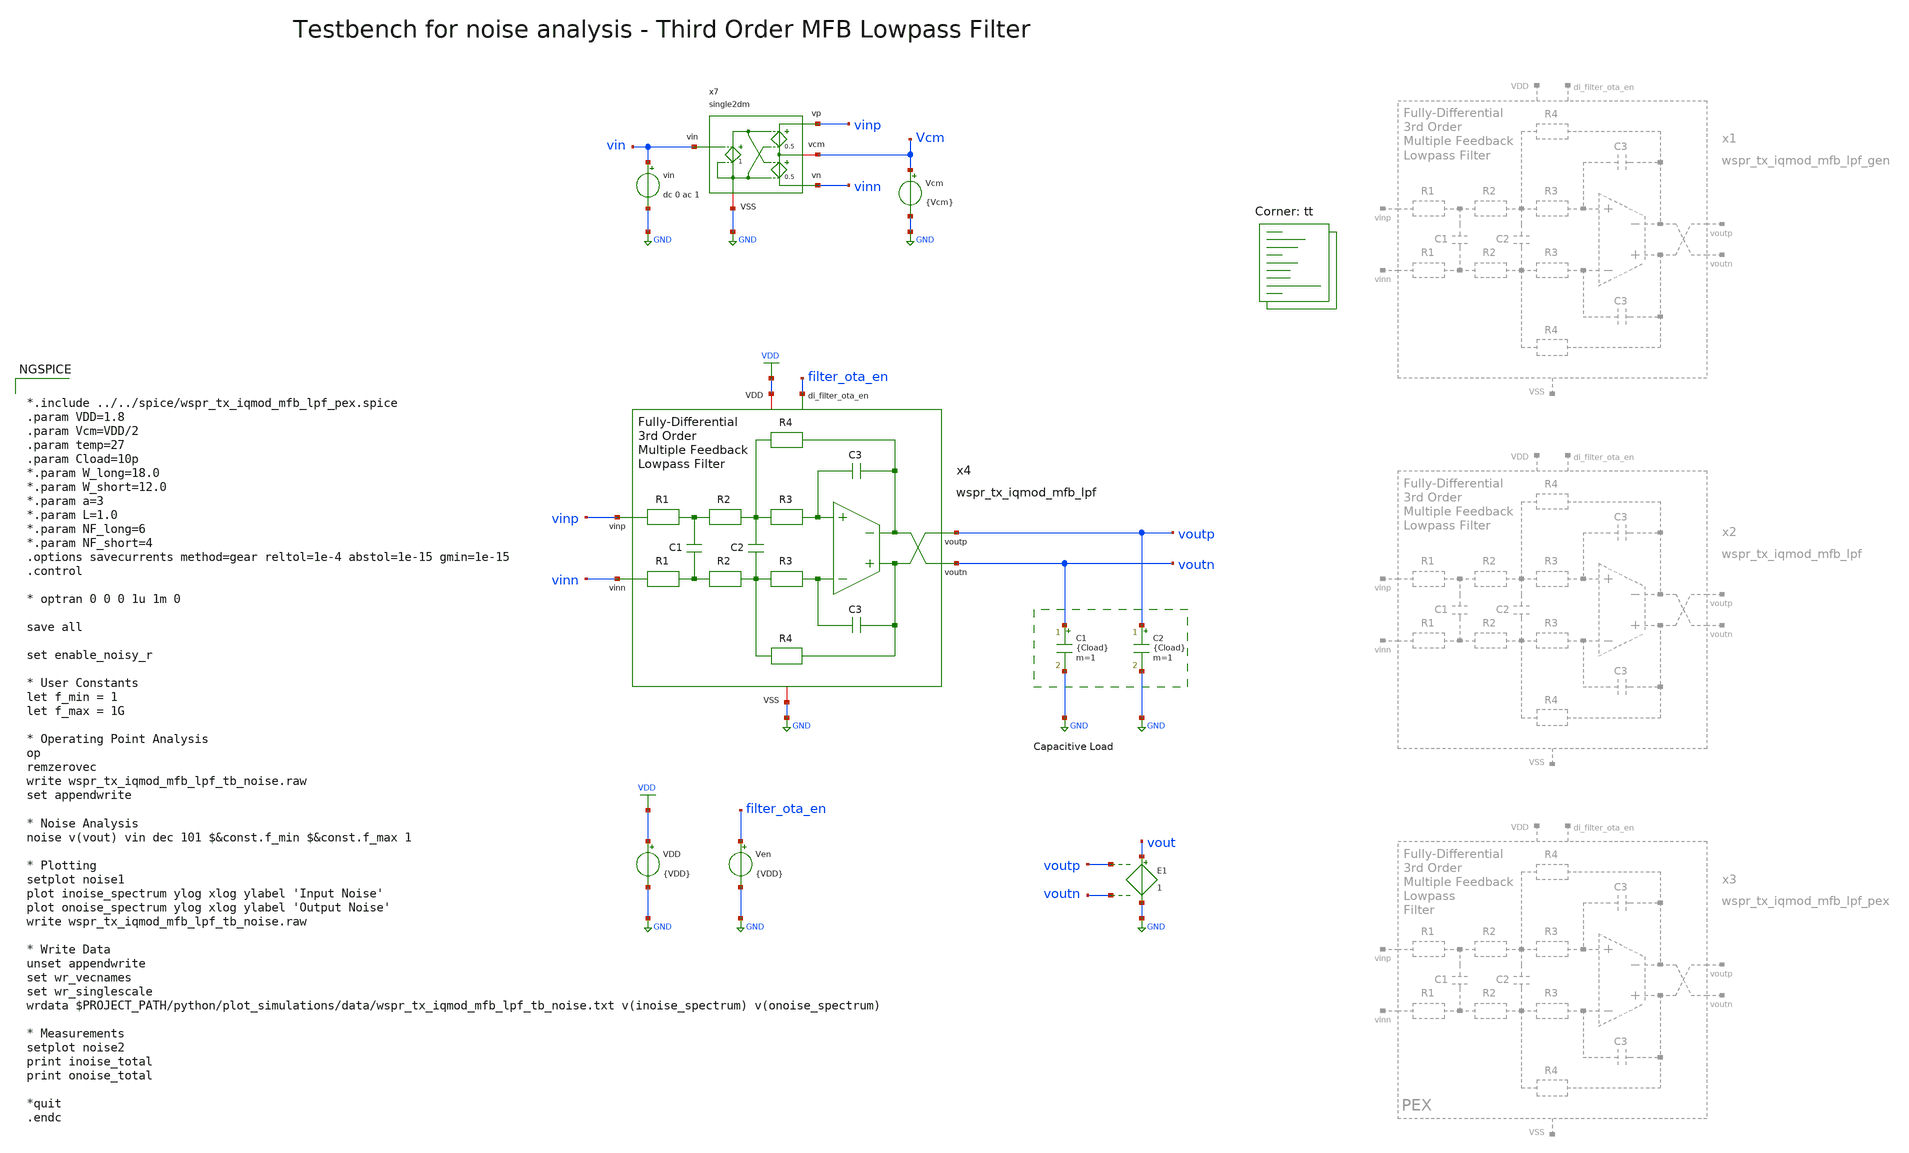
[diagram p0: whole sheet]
** sch_path: sky130/xschem/testbenches/wspr_tx_iqmod_mfb_lpf_tb_noise.sch
**.subckt wspr_tx_iqmod_mfb_lpf_tb_noise
VDD VDD GND {VDD}
C1 voutn GND {Cload} m=1
C2 voutp GND {Cload} m=1
Ven filter_ota_en GND {VDD}
E1 vout GND voutp voutn 1
x4 filter_ota_en voutp vinp voutn vinn VDD GND wspr_tx_iqmod_mfb_lpf
Vcm Vcm GND {Vcm}
vin vin GND dc 0 ac 1
x7 vinp vin Vcm GND vinn single2dm
**** begin user architecture code


*.include ../../spice/wspr_tx_iqmod_mfb_lpf_pex.spice
.param VDD=1.8
.param Vcm=VDD/2
.param temp=27
.param Cload=10p
*.param W_long=18.0
*.param W_short=12.0
*.param a=3
*.param L=1.0
*.param NF_long=6
*.param NF_short=4
.options savecurrents method=gear reltol=1e-4 abstol=1e-15 gmin=1e-15
.control

* optran 0 0 0 1u 1m 0

save all

set enable_noisy_r

* User Constants
let f_min = 1
let f_max = 1G

* Operating Point Analysis
op
remzerovec
write wspr_tx_iqmod_mfb_lpf_tb_noise.raw
set appendwrite

* Noise Analysis
noise v(vout) vin dec 101 $&const.f_min $&const.f_max 1

* Plotting
setplot noise1
plot inoise_spectrum ylog xlog ylabel 'Input Noise'
plot onoise_spectrum ylog xlog ylabel 'Output Noise'
write wspr_tx_iqmod_mfb_lpf_tb_noise.raw

* Write Data
unset appendwrite
set wr_vecnames
set wr_singlescale
wrdata $PROJECT_PATH/python/plot_simulations/data/wspr_tx_iqmod_mfb_lpf_tb_noise.txt
+ v(inoise_spectrum) v(onoise_spectrum)

* Measurements
setplot noise2
print inoise_total
print onoise_total

*quit
.endc


.lib $::SKYWATER_MODELS/sky130.lib.spice tt
**** end user architecture code
**.ends
.GLOBAL GND
.GLOBAL VDD
.end
